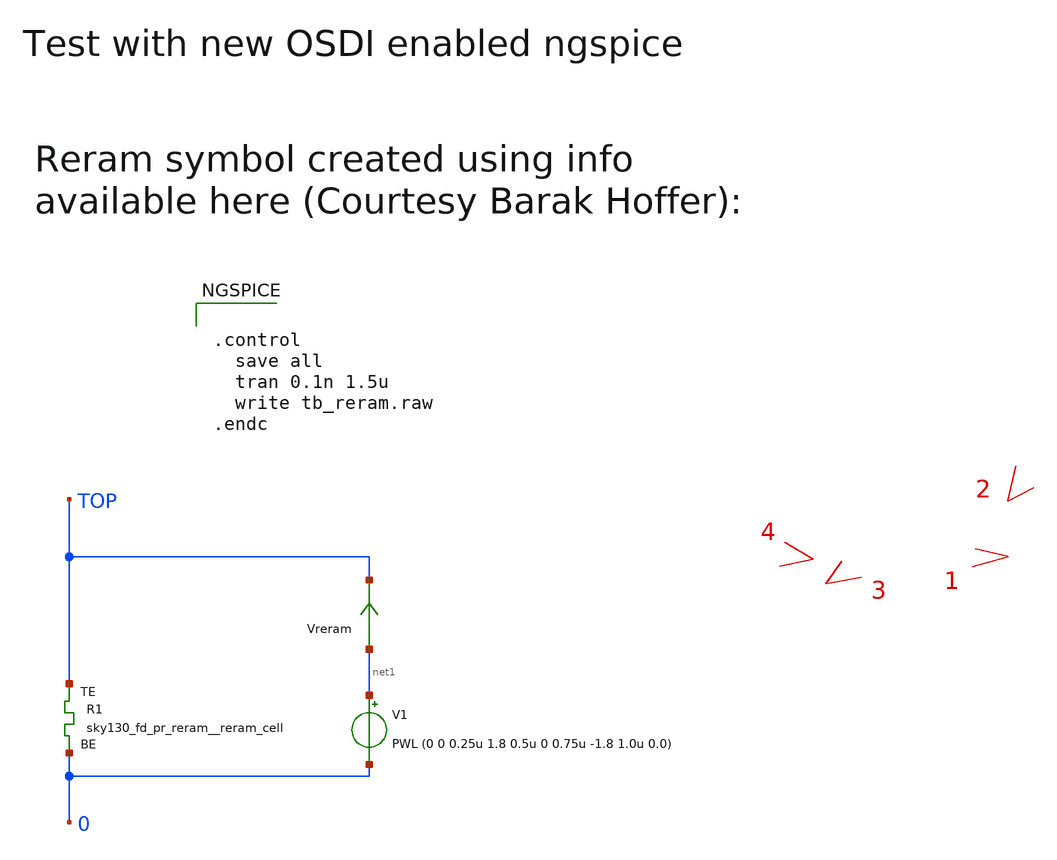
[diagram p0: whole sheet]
** sch_path: sky130_tests/tb_reram.sch
* Copyright 2021 Stefan Frederik Schippers
* Licensed under the Apache License, Version 2.0 (the "License");
* you may not use this file except in compliance with the License.
* You may obtain a copy of the License at
* https://www.apache.org/licenses/LICENSE-2.0
* Unless required by applicable law or agreed to in writing, software
* distributed under the License is distributed on an "AS IS" BASIS,
* WITHOUT WARRANTIES OR CONDITIONS OF ANY KIND, either express or implied.
* See the License for the specific language governing permissions and
* limitations under the License.
**.subckt tb_reram
V1 net1 0 PWL (0 0 0.25u 1.8 0.5u 0 0.75u -1.8 1.0u 0.0)
R1 0 TOP sky130_fd_pr_reram__reram_cell m=1
Vreram net1 TOP 0
.save i(vreram)
**** begin user architecture code


.control
  save all
  tran 0.1n 1.5u
  write tb_reram.raw
.endc



**** end user architecture code
**.ends
**** begin user architecture code
.model rram2_model rram2 rram2_params.scs
**** end user architecture code
.end
